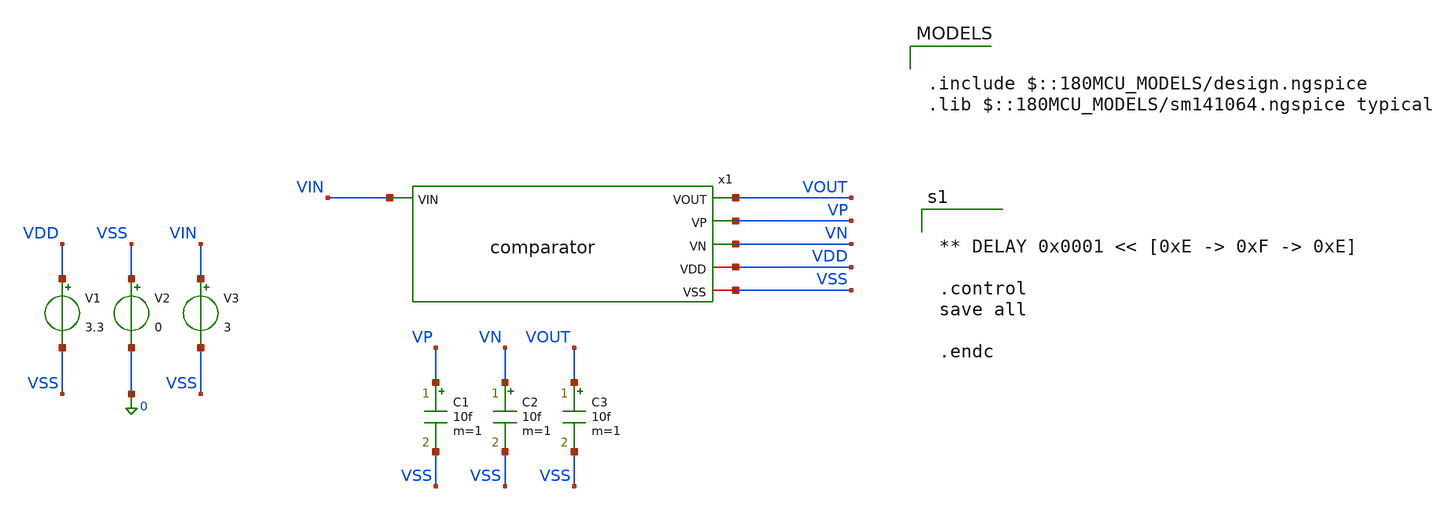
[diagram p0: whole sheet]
** sch_path: analog/schmitt_trigger_comparator/schmitt_trigger_comparator_testbench.sch
**.subckt schmitt_trigger_comparator_testbench
x1 VIN VOUT VP VN VDD VSS comparator
V1 VDD VSS 3.3
V2 VSS 0 0
V3 VIN VSS 3
C1 VP VSS 10f m=1
C2 VN VSS 10f m=1
C3 VOUT VSS 10f m=1
**** begin user architecture code

.include $::180MCU_MODELS/design.ngspice
.lib $::180MCU_MODELS/sm141064.ngspice typical



** DELAY 0x0001 << [0xE -> 0xF -> 0xE]

.control
save all

.endc


**** end user architecture code
**.ends
.end
